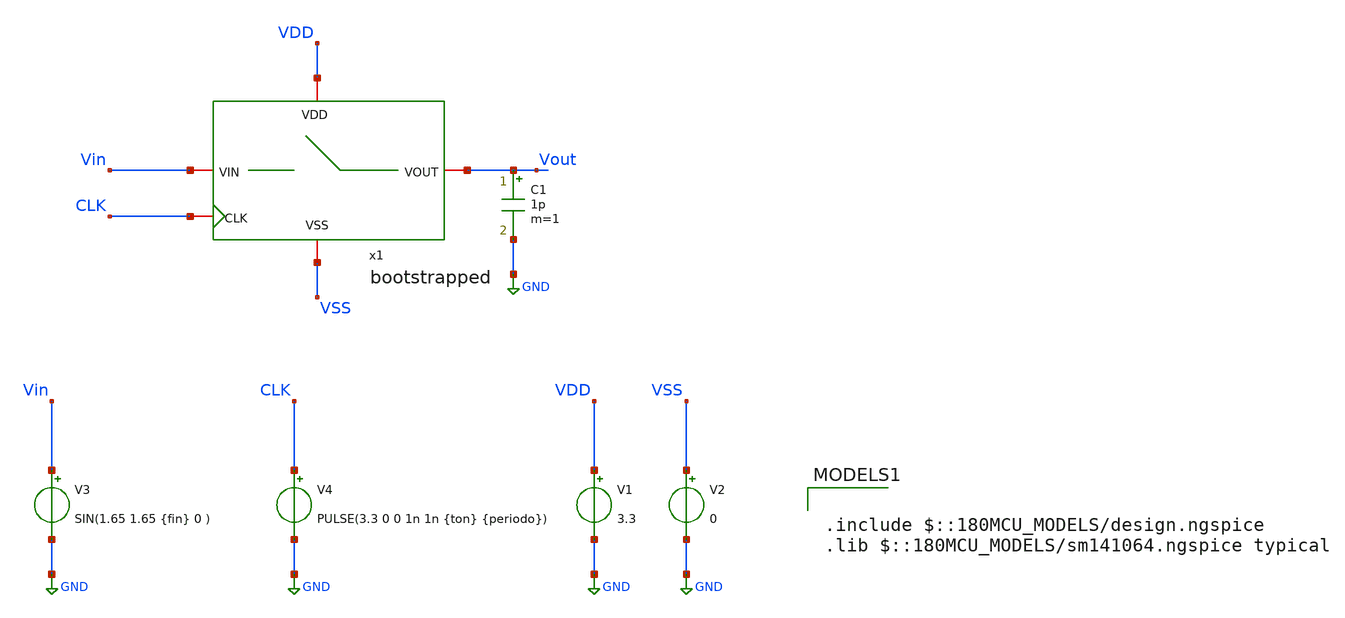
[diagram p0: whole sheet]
** sch_path: designs/sar_adc/samplehold/bootstrapped/xschem/tb_bootstrapped.sch
**.subckt tb_bootstrapped
V1 VDD GND 3.3
V2 VSS GND 0
V3 Vin GND SIN(1.65 1.65 {fin} 0 )
V4 CLK GND PULSE(3.3 0 0 1n 1n {ton} {periodo})
C1 Vout GND 1p m=1
x1 VDD VSS CLK Vin Vout bootstrapped
**** begin user architecture code

.include $::180MCU_MODELS/design.ngspice
.lib $::180MCU_MODELS/sm141064.ngspice typical



.param Fs = 5Meg
.param ton=periodo/2
.param periodo=1/fs
.param Ns = 1024
.param Nc = 103
.param fin = Nc/Ns*Fs


.control
    save all

    tran 0.2n 204.8u
    fourier  {fin} v(vout)
    plot v(vout) v(vin) xl 0 4u
    setplot tran1
    setscale time
    set wr_singlescale
    set wr_vecnames
    option numdgt=6
    wrdata ~/Desktop/sample_holf/datos_simulacion.txt vout vin

    linearize v(vout) v(vin)
    set specwindow=Blackman
    fft v(vout) v(vin)
    plot db(mag(v(vout))) xl 100k 2.5Meg

.endc



**** end user architecture code
**.ends
.GLOBAL GND
.end
